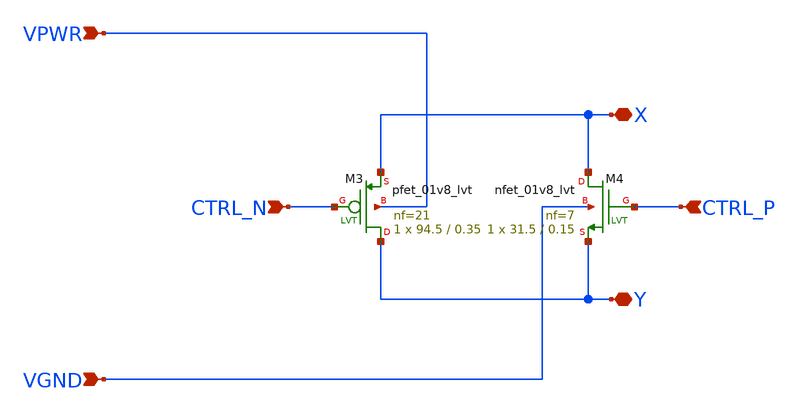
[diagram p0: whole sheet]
** sch_path: swtch_gate_sky130nm/design/SWTCH_GATE_SKY130NM/SWTCH_GATE.sch
**.subckt SWTCH_GATE VPWR VGND CTRL_P CTRL_N X Y
*.ipin VPWR
*.ipin VGND
*.ipin CTRL_P
*.ipin CTRL_N
*.iopin X
*.iopin Y
XM3 Y CTRL_N X VPWR sky130_fd_pr__pfet_01v8_lvt L=0.35 W=94.5 nf=21 ad='int((nf+1)/2) * W/nf * 0.29'
+ as='int((nf+2)/2) * W/nf * 0.29' pd='2*int((nf+1)/2) * (W/nf + 0.29)' ps='2*int((nf+2)/2) * (W/nf + 0.29)'
+ nrd='0.29 / W' nrs='0.29 / W' sa=0 sb=0 sd=0 mult=1 m=1
XM4 X CTRL_P Y VGND sky130_fd_pr__nfet_01v8_lvt L=0.15 W=31.5 nf=7 ad='int((nf+1)/2) * W/nf * 0.29' as='int((nf+2)/2) * W/nf * 0.29'
+ pd='2*int((nf+1)/2) * (W/nf + 0.29)' ps='2*int((nf+2)/2) * (W/nf + 0.29)' nrd='0.29 / W' nrs='0.29 / W'
+ sa=0 sb=0 sd=0 mult=1 m=1
**.ends
.end
